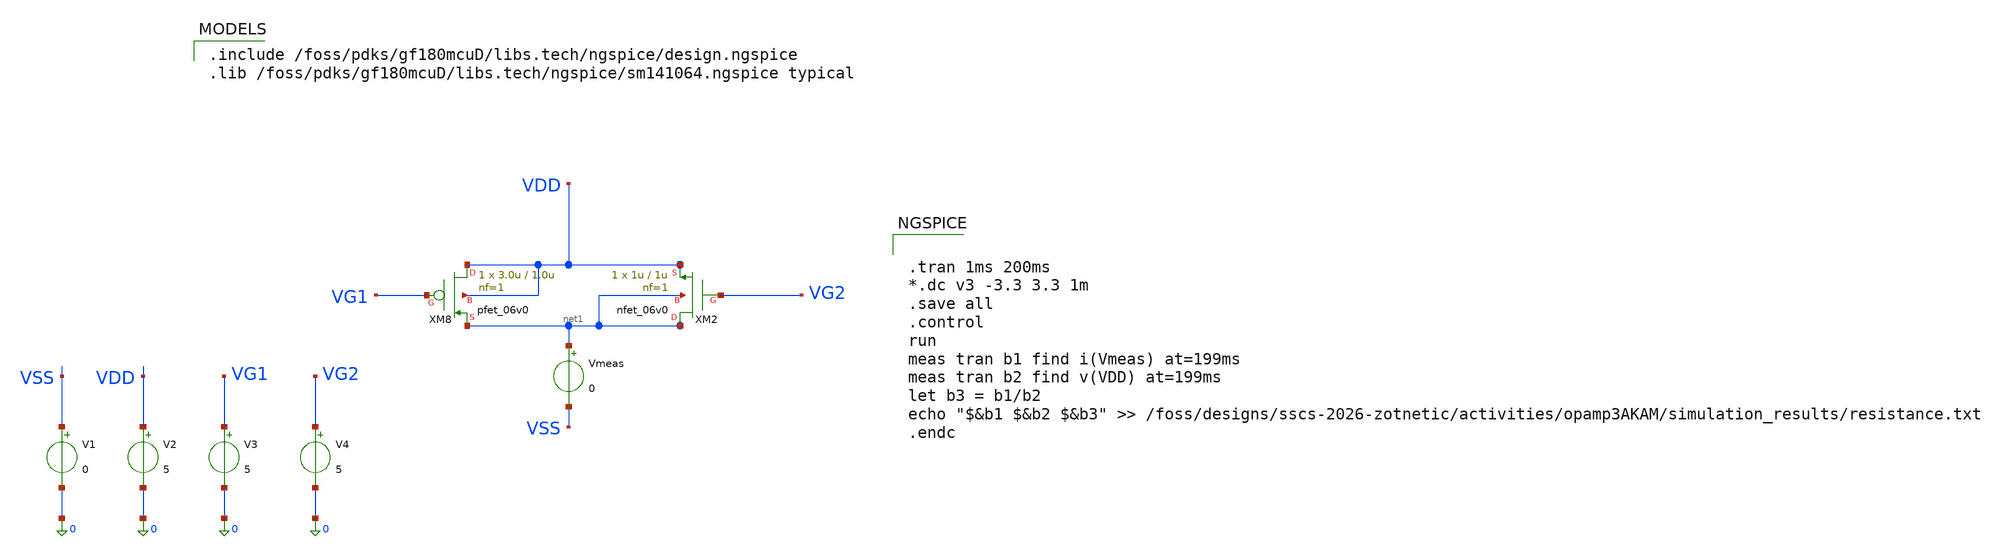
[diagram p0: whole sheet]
** sch_path: activities/opamp3AKAM/simulations_testbench/untitled-6.sch
**.subckt untitled-6
XM2 net1 VG2 VDD net1 nfet_06v0 L=1u W=1u nf=1 ad='int((nf+1)/2) * W/nf * 0.18u' as='int((nf+2)/2) * W/nf * 0.18u'
+ pd='2*int((nf+1)/2) * (W/nf + 0.18u)' ps='2*int((nf+2)/2) * (W/nf + 0.18u)' nrd='0.18u / W' nrs='0.18u / W'
+ sa=0 sb=0 sd=0 m=1
XM8 VDD VG1 net1 VDD pfet_06v0 L=1.0u W=3.0u nf=1 ad='int((nf+1)/2) * W/nf * 0.18u' as='int((nf+2)/2) * W/nf * 0.18u'
+ pd='2*int((nf+1)/2) * (W/nf + 0.18u)' ps='2*int((nf+2)/2) * (W/nf + 0.18u)' nrd='0.18u / W' nrs='0.18u / W'
+ sa=0 sb=0 sd=0 m=1
V1 VSS 0 0
V2 VDD 0 5
V3 VG1 0 5
V4 VG2 0 5
Vmeas net1 VSS 0
**** begin user architecture code

.include /foss/pdks/gf180mcuD/libs.tech/ngspice/design.ngspice
.lib /foss/pdks/gf180mcuD/libs.tech/ngspice/sm141064.ngspice typical



.tran 1ms 200ms
*.dc v3 -3.3 3.3 1m
.save all
.control
run
meas tran b1 find i(Vmeas) at=199ms
meas tran b2 find v(VDD) at=199ms
let b3 = b1/b2
echo "$&b1 $&b2 $&b3" >>
+ /foss/designs/sscs-2026-zotnetic/activities/opamp3AKAM/simulation_results/resistance.txt
.endc

**** end user architecture code
**.ends
.end
